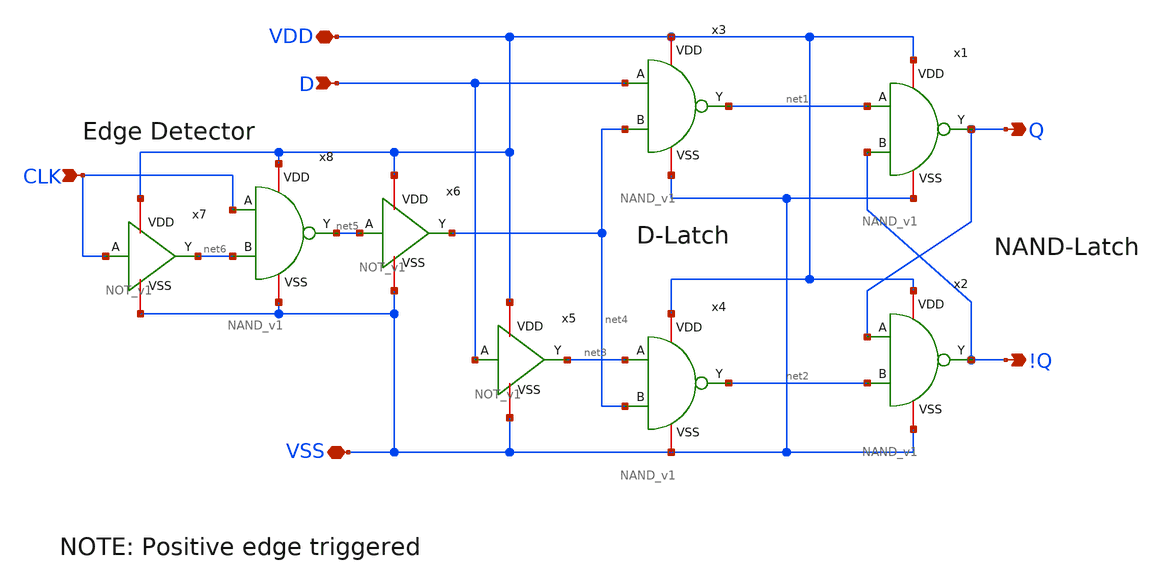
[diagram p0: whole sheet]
** sch_path: team_src/xschem/D_FF_v1.sch
**.subckt D_FF_v1 CLK D VDD Q !Q VSS
*.ipin CLK
*.ipin D
*.iopin VDD
*.opin Q
*.opin !Q
*.iopin VSS
x1 VDD Q net1 !Q VSS NAND_v1
x2 VDD !Q Q net2 VSS NAND_v1
x3 VDD net1 D net4 VSS NAND_v1
x4 VDD net2 net3 net4 VSS NAND_v1
x5 VDD D net3 VSS NOT_v1
x6 VDD net5 net4 VSS NOT_v1
x7 VDD CLK net6 VSS NOT_v1
x8 VDD net5 CLK net6 VSS NAND_v1
**.ends

* expanding   symbol:  NAND_v1.sym # of pins=5
** sym_path: team_src/xschem/NAND_v1.sym
** sch_path: team_src/xschem/NAND_v1.sch
.subckt NAND_v1 VDD Y A B VSS
*.iopin VSS
*.iopin VDD
*.ipin A
*.opin Y
*.ipin B
XM1 net1 B VSS VSS nfet_03v3 L=0.28u W=1u nf=1 ad='int((nf+1)/2) * W/nf * 0.18u' as='int((nf+2)/2) * W/nf * 0.18u'
+ pd='2*int((nf+1)/2) * (W/nf + 0.18u)' ps='2*int((nf+2)/2) * (W/nf + 0.18u)' nrd='0.18u / W' nrs='0.18u / W'
+ sa=0 sb=0 sd=0 m=1
XM2 Y A net1 net1 nfet_03v3 L=0.28u W=1u nf=1 ad='int((nf+1)/2) * W/nf * 0.18u' as='int((nf+2)/2) * W/nf * 0.18u'
+ pd='2*int((nf+1)/2) * (W/nf + 0.18u)' ps='2*int((nf+2)/2) * (W/nf + 0.18u)' nrd='0.18u / W' nrs='0.18u / W'
+ sa=0 sb=0 sd=0 m=1
XM3 Y B VDD VDD pfet_03v3 L=0.28u W=1u nf=1 ad='int((nf+1)/2) * W/nf * 0.18u' as='int((nf+2)/2) * W/nf * 0.18u'
+ pd='2*int((nf+1)/2) * (W/nf + 0.18u)' ps='2*int((nf+2)/2) * (W/nf + 0.18u)' nrd='0.18u / W' nrs='0.18u / W'
+ sa=0 sb=0 sd=0 m=1
XM4 Y A VDD VDD pfet_03v3 L=0.28u W=1u nf=1 ad='int((nf+1)/2) * W/nf * 0.18u' as='int((nf+2)/2) * W/nf * 0.18u'
+ pd='2*int((nf+1)/2) * (W/nf + 0.18u)' ps='2*int((nf+2)/2) * (W/nf + 0.18u)' nrd='0.18u / W' nrs='0.18u / W'
+ sa=0 sb=0 sd=0 m=1
.ends


* expanding   symbol:  NOT_v1.sym # of pins=4
** sym_path: team_src/xschem/NOT_v1.sym
** sch_path: team_src/xschem/NOT_v1.sch
.subckt NOT_v1 VDD A Y VSS
*.iopin VSS
*.iopin VDD
*.ipin A
*.opin Y
XM2 Y A VSS net1 nfet_03v3 L=0.28u W=1u nf=1 ad='int((nf+1)/2) * W/nf * 0.18u' as='int((nf+2)/2) * W/nf * 0.18u'
+ pd='2*int((nf+1)/2) * (W/nf + 0.18u)' ps='2*int((nf+2)/2) * (W/nf + 0.18u)' nrd='0.18u / W' nrs='0.18u / W'
+ sa=0 sb=0 sd=0 m=1
XM4 Y A VDD net2 pfet_03v3 L=0.28u W=1u nf=1 ad='int((nf+1)/2) * W/nf * 0.18u' as='int((nf+2)/2) * W/nf * 0.18u'
+ pd='2*int((nf+1)/2) * (W/nf + 0.18u)' ps='2*int((nf+2)/2) * (W/nf + 0.18u)' nrd='0.18u / W' nrs='0.18u / W'
+ sa=0 sb=0 sd=0 m=1
.ends

.end
